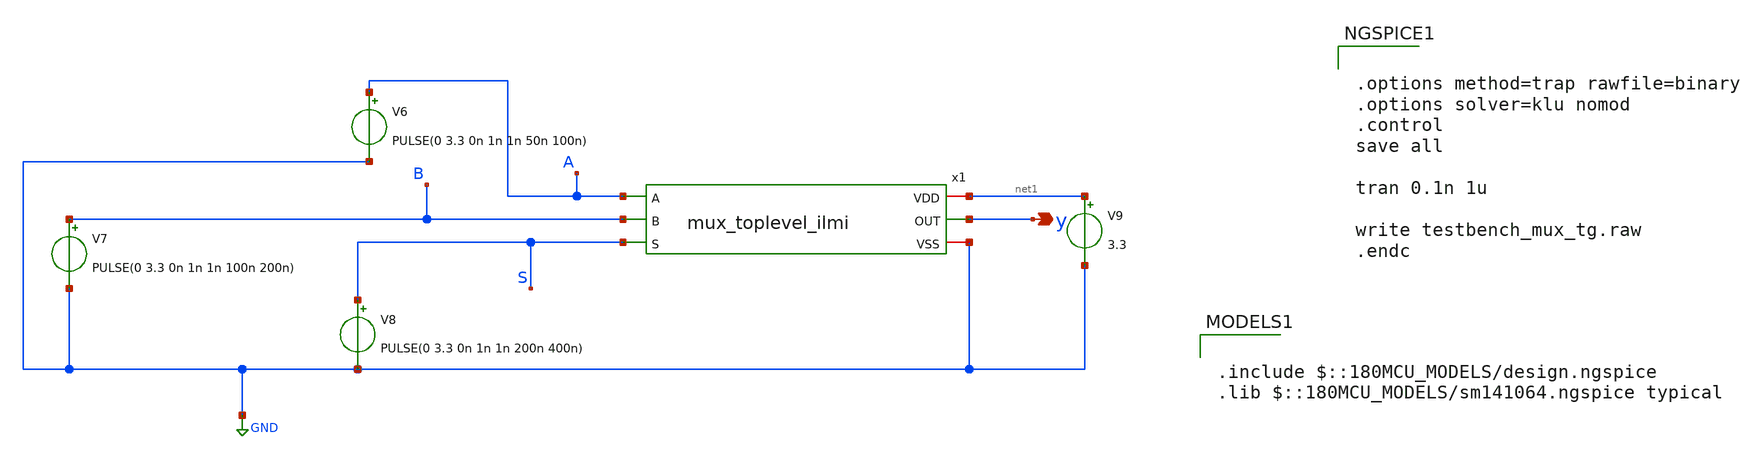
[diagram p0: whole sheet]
** sch_path: designs/libs/core_fpga/mux2x1_transmission_gate/testbench_mux_tg.sch
**.subckt testbench_mux_tg y
*.opin y
V6 A GND PULSE(0 3.3 0n 1n 1n 50n 100n)
V7 B GND PULSE(0 3.3 0n 1n 1n 100n 200n)
V8 S GND PULSE(0 3.3 0n 1n 1n 200n 400n)
V9 net1 GND 3.3
x1 net1 A y B GND S mux_toplevel_ilmi
**** begin user architecture code

.include $::180MCU_MODELS/design.ngspice
.lib $::180MCU_MODELS/sm141064.ngspice typical



.options method=trap rawfile=binary
.options solver=klu nomod
.control
save all

tran 0.1n 1u

write testbench_mux_tg.raw
.endc


**** end user architecture code
**.ends
.GLOBAL GND
.end
